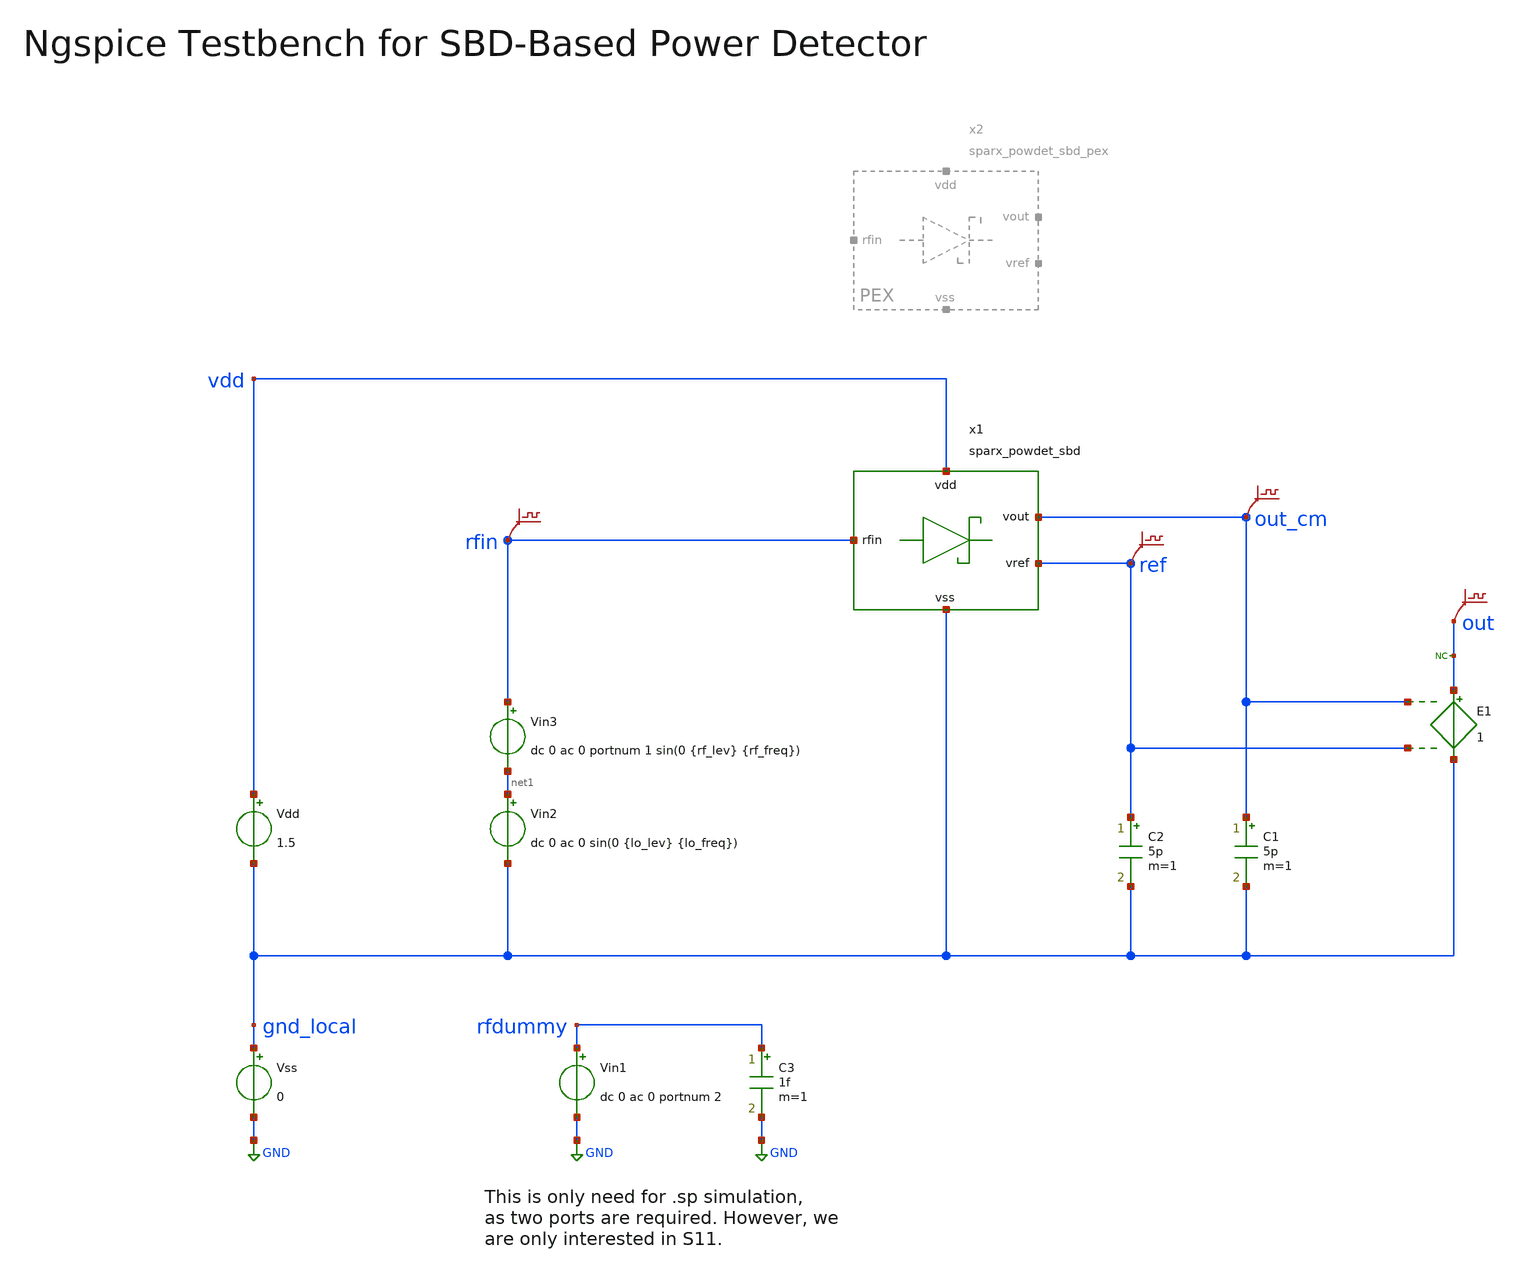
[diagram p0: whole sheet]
** sch_path: testbenches/sparx_powdet_sbd_tb.sch
* (c) 2026 H. Pretl, ICD@JKU
**.subckt sparx_powdet_sbd_tb
Vss gnd_local GND 0
Vin3 rfin net1 dc 0 ac 0 portnum 1 sin(0 {rf_lev} {rf_freq})
Vin1 rfdummy GND dc 0 ac 0 portnum 2
C3 rfdummy GND 1f m=1
.save v(rfin)
.save v(out_cm)
Vin2 net1 gnd_local dc 0 ac 0 sin(0 {lo_lev} {lo_freq})
Vdd vdd gnd_local 1.5
.save v(ref)
C1 out_cm gnd_local 5p m=1
C2 ref gnd_local 5p m=1
E1 out gnd_local out_cm ref 1
.save v(out)
* noconn out
x1 out_cm ref vdd rfin gnd_local sparx_powdet_sbd
**** begin user architecture code

.lib cornerDIO.lib dio_tt
.lib cornerMOSlv.lib mos_tt
.lib cornerRES.lib res_typ
.lib cornerCAP.lib cap_typ



.include ../../netlist/pex/sparx_powdet_sbd_magic_pex.spice
* .include ../../netlist/pex/sparx_powdet_sbd_klayout_pex.spice
.temp 27
.option method=gear
.save all
.include sparx_powdet_sbd_tb.save
.param lo_freq=149G
.param lo_lev=100m
.param rf_freq=151G
.param rf_lev=1m
.control
set num_threads=8
*set specwindow=blackman

let lo_freq = 149G
let rf_freq = 151G
let if_freq = rf_freq - lo_freq

op
write sparx_powdet_sbd_tb.raw
set appendwrite

sp lin 31 100G 200G 0
write sparx_powdet_sbd_tb.raw

ac dec 1001 1MEG 10G
write sparx_powdet_sbd_tb.raw

tran 0.05p 22n 20n
write sparx_powdet_sbd_tb.raw

linearize rfin out
setplot tran2
fft rfin
plot db(rfin)
meas sp lo_tone FIND v(rfin) AT=$&lo_freq
meas sp rf_tone FIND v(rfin) AT=$&rf_freq
print lo_tone > result.txt
print rf_tone >> result.txt
setplot tran2
fft out
plot db(out)
meas sp if_tone FIND v(out) AT=$&if_freq
print if_tone >> result.txt

*exit
.endc


**** end user architecture code
**.ends
.GLOBAL GND
.end
